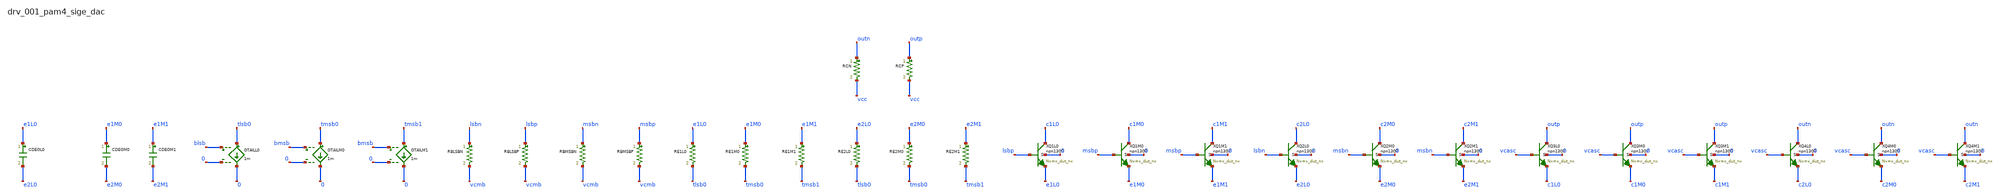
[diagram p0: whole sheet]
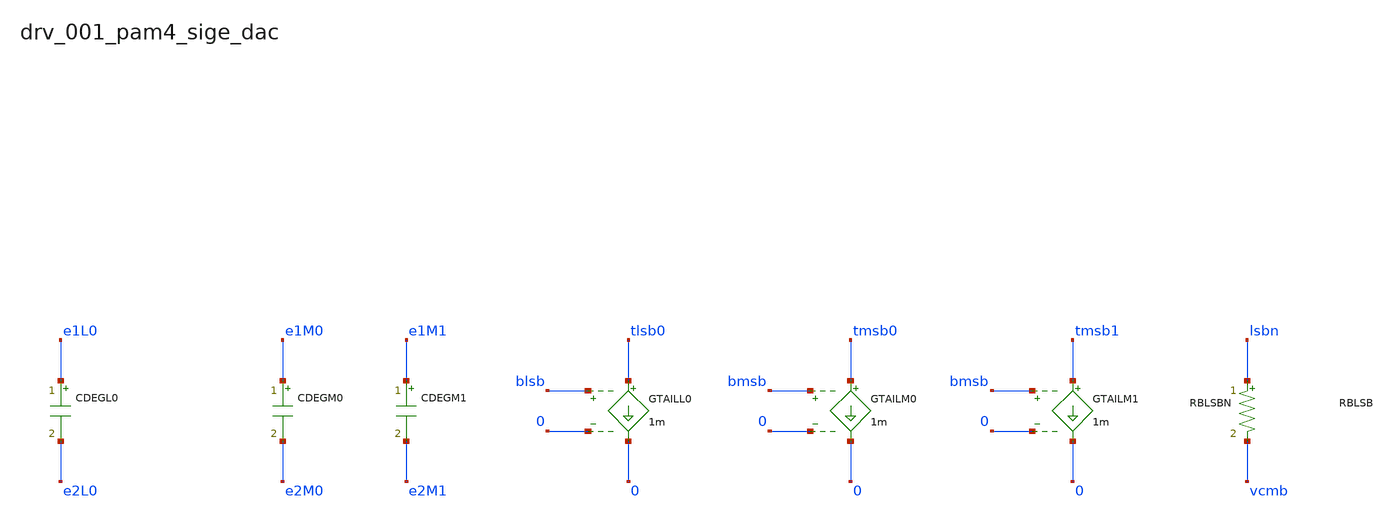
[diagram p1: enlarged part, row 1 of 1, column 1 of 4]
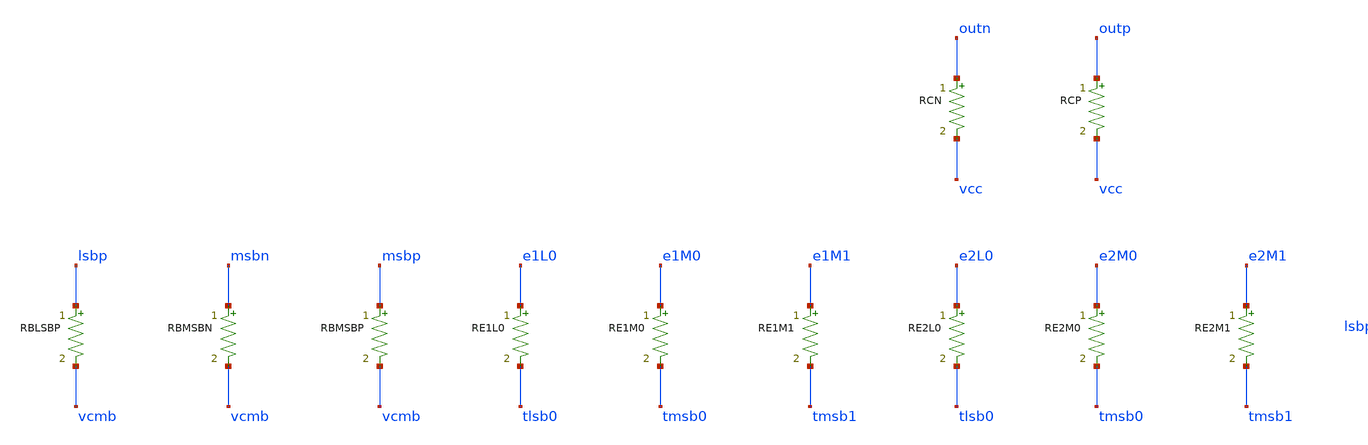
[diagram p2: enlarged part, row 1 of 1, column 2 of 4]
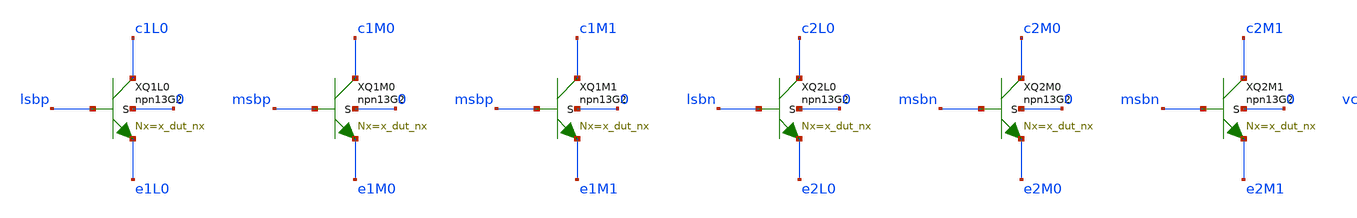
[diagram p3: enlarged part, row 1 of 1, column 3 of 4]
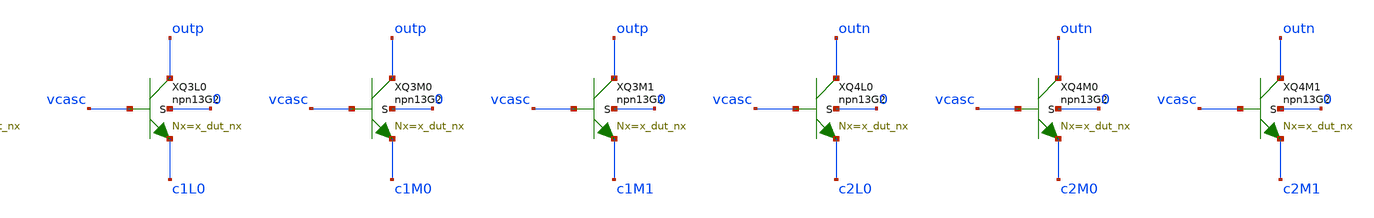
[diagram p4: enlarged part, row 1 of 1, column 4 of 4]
** sch_path: analog-db/raw/drv_001_pam4_sige_dac/hier/drv_001_pam4_sige_dac.sch
**.subckt drv_001_pam4_sige_dac
CDEGL0 e1L0 e2L0 {x_dut_cdeg_ff*1f} m=1
CDEGM0 e1M0 e2M0 {x_dut_cdeg_ff*1f} m=1
CDEGM1 e1M1 e2M1 {x_dut_cdeg_ff*1f} m=1
GTAILL0 tlsb0 0 blsb 0 1m
GTAILM0 tmsb0 0 bmsb 0 1m
GTAILM1 tmsb1 0 bmsb 0 1m
RBLSBN lsbn vcmb {x_dut_rb} m=1
RBLSBP lsbp vcmb {x_dut_rb} m=1
RBMSBN msbn vcmb {x_dut_rb} m=1
RBMSBP msbp vcmb {x_dut_rb} m=1
RCN outn vcc {x_dut_rc} m=1
RCP outp vcc {x_dut_rc} m=1
RE1L0 e1L0 tlsb0 {x_dut_re} m=1
RE1M0 e1M0 tmsb0 {x_dut_re} m=1
RE1M1 e1M1 tmsb1 {x_dut_re} m=1
RE2L0 e2L0 tlsb0 {x_dut_re} m=1
RE2M0 e2M0 tmsb0 {x_dut_re} m=1
RE2M1 e2M1 tmsb1 {x_dut_re} m=1
XQ1L0 c1L0 lsbp e1L0 0 npn13G2 Nx=x_dut_nx
XQ1M0 c1M0 msbp e1M0 0 npn13G2 Nx=x_dut_nx
XQ1M1 c1M1 msbp e1M1 0 npn13G2 Nx=x_dut_nx
XQ2L0 c2L0 lsbn e2L0 0 npn13G2 Nx=x_dut_nx
XQ2M0 c2M0 msbn e2M0 0 npn13G2 Nx=x_dut_nx
XQ2M1 c2M1 msbn e2M1 0 npn13G2 Nx=x_dut_nx
XQ3L0 outp vcasc c1L0 0 npn13G2 Nx=x_dut_nx
XQ3M0 outp vcasc c1M0 0 npn13G2 Nx=x_dut_nx
XQ3M1 outp vcasc c1M1 0 npn13G2 Nx=x_dut_nx
XQ4L0 outn vcasc c2L0 0 npn13G2 Nx=x_dut_nx
XQ4M0 outn vcasc c2M0 0 npn13G2 Nx=x_dut_nx
XQ4M1 outn vcasc c2M1 0 npn13G2 Nx=x_dut_nx
**.ends
.end
